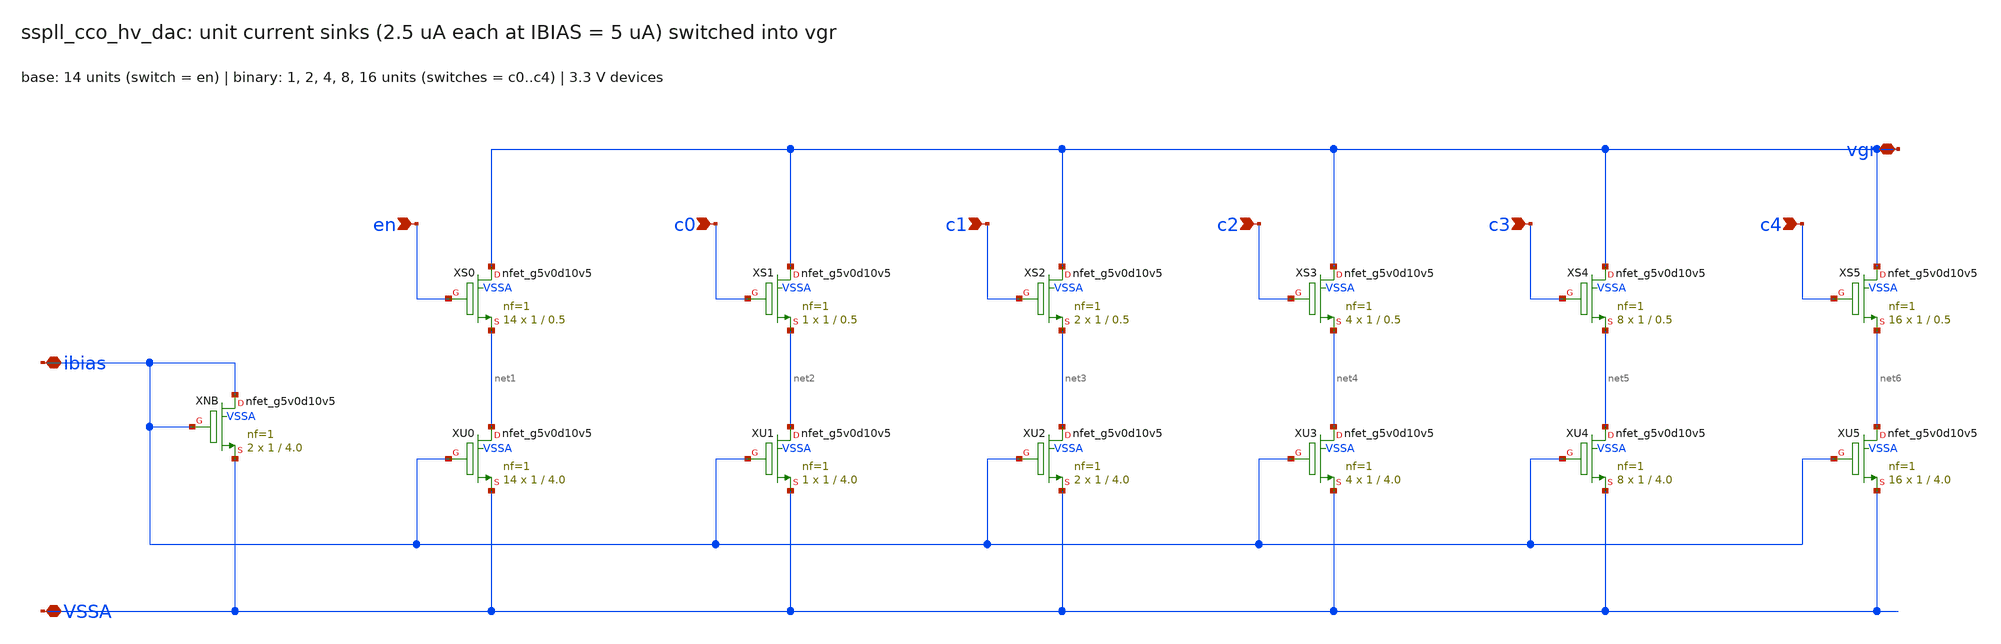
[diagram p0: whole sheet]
** sch_path: xschem/cco_hv/sspll_cco_hv_dac.sch
**.subckt sspll_cco_hv_dac ibias VSSA en c0 c1 c2 c3 c4 vgr
*.iopin ibias
*.iopin VSSA
*.ipin en
*.ipin c0
*.ipin c1
*.ipin c2
*.ipin c3
*.ipin c4
*.iopin vgr
XXNB ibias ibias VSSA VSSA sky130_fd_pr__nfet_g5v0d10v5 L=4.0 W=1 nf=1 ad='int((nf+1)/2) * W/nf * 0.29'
+ as='int((nf+2)/2) * W/nf * 0.29' pd='2*int((nf+1)/2) * (W/nf + 0.29)' ps='2*int((nf+2)/2) * (W/nf + 0.29)'
+ nrd='0.29 / W' nrs='0.29 / W' sa=0 sb=0 sd=0 mult=2 m=2
XXS0 vgr en net1 VSSA sky130_fd_pr__nfet_g5v0d10v5 L=0.5 W=1 nf=1 ad='int((nf+1)/2) * W/nf * 0.29' as='int((nf+2)/2) * W/nf * 0.29'
+ pd='2*int((nf+1)/2) * (W/nf + 0.29)' ps='2*int((nf+2)/2) * (W/nf + 0.29)' nrd='0.29 / W' nrs='0.29 / W'
+ sa=0 sb=0 sd=0 mult=14 m=14
XXU0 net1 ibias VSSA VSSA sky130_fd_pr__nfet_g5v0d10v5 L=4.0 W=1 nf=1 ad='int((nf+1)/2) * W/nf * 0.29'
+ as='int((nf+2)/2) * W/nf * 0.29' pd='2*int((nf+1)/2) * (W/nf + 0.29)' ps='2*int((nf+2)/2) * (W/nf + 0.29)'
+ nrd='0.29 / W' nrs='0.29 / W' sa=0 sb=0 sd=0 mult=14 m=14
XXS1 vgr c0 net2 VSSA sky130_fd_pr__nfet_g5v0d10v5 L=0.5 W=1 nf=1 ad='int((nf+1)/2) * W/nf * 0.29' as='int((nf+2)/2) * W/nf * 0.29'
+ pd='2*int((nf+1)/2) * (W/nf + 0.29)' ps='2*int((nf+2)/2) * (W/nf + 0.29)' nrd='0.29 / W' nrs='0.29 / W'
+ sa=0 sb=0 sd=0 mult=1 m=1
XXU1 net2 ibias VSSA VSSA sky130_fd_pr__nfet_g5v0d10v5 L=4.0 W=1 nf=1 ad='int((nf+1)/2) * W/nf * 0.29'
+ as='int((nf+2)/2) * W/nf * 0.29' pd='2*int((nf+1)/2) * (W/nf + 0.29)' ps='2*int((nf+2)/2) * (W/nf + 0.29)'
+ nrd='0.29 / W' nrs='0.29 / W' sa=0 sb=0 sd=0 mult=1 m=1
XXS2 vgr c1 net3 VSSA sky130_fd_pr__nfet_g5v0d10v5 L=0.5 W=1 nf=1 ad='int((nf+1)/2) * W/nf * 0.29' as='int((nf+2)/2) * W/nf * 0.29'
+ pd='2*int((nf+1)/2) * (W/nf + 0.29)' ps='2*int((nf+2)/2) * (W/nf + 0.29)' nrd='0.29 / W' nrs='0.29 / W'
+ sa=0 sb=0 sd=0 mult=2 m=2
XXU2 net3 ibias VSSA VSSA sky130_fd_pr__nfet_g5v0d10v5 L=4.0 W=1 nf=1 ad='int((nf+1)/2) * W/nf * 0.29'
+ as='int((nf+2)/2) * W/nf * 0.29' pd='2*int((nf+1)/2) * (W/nf + 0.29)' ps='2*int((nf+2)/2) * (W/nf + 0.29)'
+ nrd='0.29 / W' nrs='0.29 / W' sa=0 sb=0 sd=0 mult=2 m=2
XXS3 vgr c2 net4 VSSA sky130_fd_pr__nfet_g5v0d10v5 L=0.5 W=1 nf=1 ad='int((nf+1)/2) * W/nf * 0.29' as='int((nf+2)/2) * W/nf * 0.29'
+ pd='2*int((nf+1)/2) * (W/nf + 0.29)' ps='2*int((nf+2)/2) * (W/nf + 0.29)' nrd='0.29 / W' nrs='0.29 / W'
+ sa=0 sb=0 sd=0 mult=4 m=4
XXU3 net4 ibias VSSA VSSA sky130_fd_pr__nfet_g5v0d10v5 L=4.0 W=1 nf=1 ad='int((nf+1)/2) * W/nf * 0.29'
+ as='int((nf+2)/2) * W/nf * 0.29' pd='2*int((nf+1)/2) * (W/nf + 0.29)' ps='2*int((nf+2)/2) * (W/nf + 0.29)'
+ nrd='0.29 / W' nrs='0.29 / W' sa=0 sb=0 sd=0 mult=4 m=4
XXS4 vgr c3 net5 VSSA sky130_fd_pr__nfet_g5v0d10v5 L=0.5 W=1 nf=1 ad='int((nf+1)/2) * W/nf * 0.29' as='int((nf+2)/2) * W/nf * 0.29'
+ pd='2*int((nf+1)/2) * (W/nf + 0.29)' ps='2*int((nf+2)/2) * (W/nf + 0.29)' nrd='0.29 / W' nrs='0.29 / W'
+ sa=0 sb=0 sd=0 mult=8 m=8
XXU4 net5 ibias VSSA VSSA sky130_fd_pr__nfet_g5v0d10v5 L=4.0 W=1 nf=1 ad='int((nf+1)/2) * W/nf * 0.29'
+ as='int((nf+2)/2) * W/nf * 0.29' pd='2*int((nf+1)/2) * (W/nf + 0.29)' ps='2*int((nf+2)/2) * (W/nf + 0.29)'
+ nrd='0.29 / W' nrs='0.29 / W' sa=0 sb=0 sd=0 mult=8 m=8
XXS5 vgr c4 net6 VSSA sky130_fd_pr__nfet_g5v0d10v5 L=0.5 W=1 nf=1 ad='int((nf+1)/2) * W/nf * 0.29' as='int((nf+2)/2) * W/nf * 0.29'
+ pd='2*int((nf+1)/2) * (W/nf + 0.29)' ps='2*int((nf+2)/2) * (W/nf + 0.29)' nrd='0.29 / W' nrs='0.29 / W'
+ sa=0 sb=0 sd=0 mult=16 m=16
XXU5 net6 ibias VSSA VSSA sky130_fd_pr__nfet_g5v0d10v5 L=4.0 W=1 nf=1 ad='int((nf+1)/2) * W/nf * 0.29'
+ as='int((nf+2)/2) * W/nf * 0.29' pd='2*int((nf+1)/2) * (W/nf + 0.29)' ps='2*int((nf+2)/2) * (W/nf + 0.29)'
+ nrd='0.29 / W' nrs='0.29 / W' sa=0 sb=0 sd=0 mult=16 m=16
**.ends
.end
